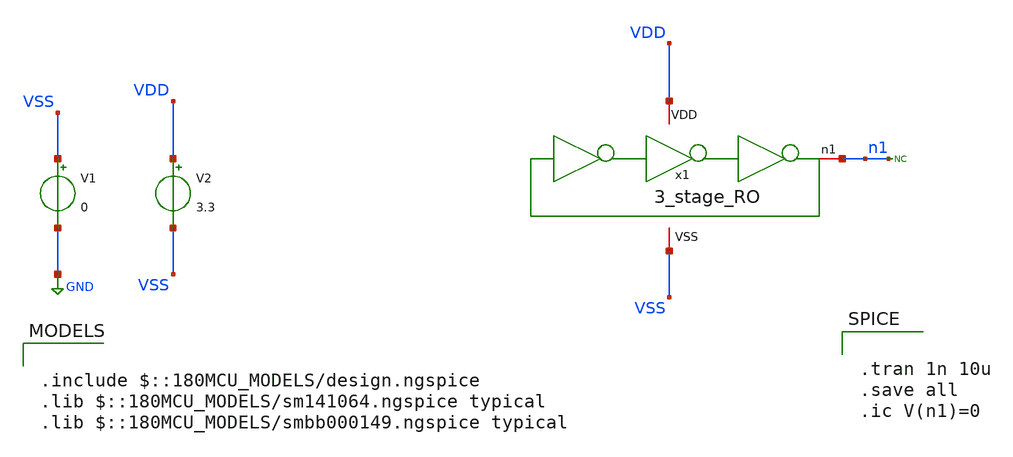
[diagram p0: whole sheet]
** sch_path: gf180_examples/RO/xschem/3_stage_RO_tb_tran.sch
**.subckt 3_stage_RO_tb_tran
x1 VDD VSS n1 3_stage_RO
V1 VSS GND 0
V2 VDD VSS 3.3
* noconn n1
**** begin user architecture code

.include $::180MCU_MODELS/design.ngspice
.lib $::180MCU_MODELS/sm141064.ngspice typical
.lib $::180MCU_MODELS/smbb000149.ngspice typical



.tran 1n 10u
.save all
.ic V(n1)=0


**** end user architecture code
**.ends

* expanding   symbol:  xschem/3_stage_RO.sym # of pins=3
** sym_path: gf180_examples/RO/xschem/3_stage_RO.sym
** sch_path: gf180_examples/RO/xschem/3_stage_RO.sch
.subckt 3_stage_RO VDD VSS n1
*.iopin VDD
*.iopin VSS
*.iopin n1
x1 n1 VDD VSS n2 inverter
x2 n2 VDD VSS n3 inverter
x3 n3 VDD VSS n1 inverter
C1 n2 VSS 100f m=1
C2 n3 VSS 100f m=1
C3 n1 VSS 100f m=1
.ends


* expanding   symbol:  /foss/designs/Chipathon2025_gf180/gf180_examples/inverter/xschem/inverter.sym
*+ # of pins=4
** sym_path: gf180_examples/inverter/xschem/inverter.sym
** sch_path: gf180_examples/inverter/xschem/inverter.sch
.subckt inverter Vin VDD VSS Vout
*.ipin Vin
*.iopin VDD
*.iopin VSS
*.iopin Vout
XM1 Vout Vin VSS VSS nfet_03v3 L=1u W=3u nf=1 ad='int((nf+1)/2) * W/nf * 0.18u' as='int((nf+2)/2) * W/nf * 0.18u'
+ pd='2*int((nf+1)/2) * (W/nf + 0.18u)' ps='2*int((nf+2)/2) * (W/nf + 0.18u)' nrd='0.18u / W' nrs='0.18u / W'
+ sa=0 sb=0 sd=0 m=1
XM2 Vout Vin VDD VDD pfet_03v3 L=1u W=3u nf=1 ad='int((nf+1)/2) * W/nf * 0.18u' as='int((nf+2)/2) * W/nf * 0.18u'
+ pd='2*int((nf+1)/2) * (W/nf + 0.18u)' ps='2*int((nf+2)/2) * (W/nf + 0.18u)' nrd='0.18u / W' nrs='0.18u / W'
+ sa=0 sb=0 sd=0 m=1
.ends

.GLOBAL GND
.end
